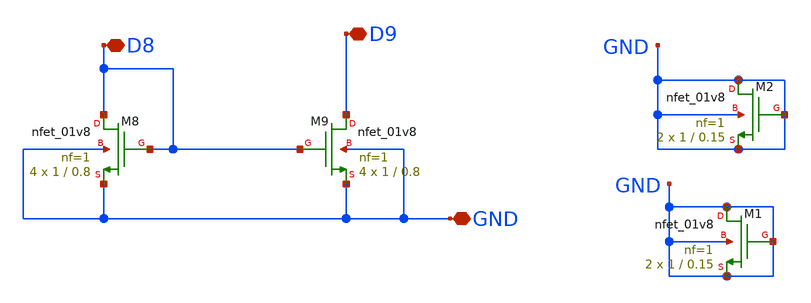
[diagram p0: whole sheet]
** sch_path: opamp/mag/nmos89.sch
**.subckt nmos89 GND D9 D8
*.iopin GND
*.iopin D9
*.iopin D8
XM8 D8 D8 GND GND sky130_fd_pr__nfet_01v8 L=0.8 W=1 nf=1 ad='int((nf+1)/2) * W/nf * 0.29' as='int((nf+2)/2) * W/nf * 0.29'
+ pd='2*int((nf+1)/2) * (W/nf + 0.29)' ps='2*int((nf+2)/2) * (W/nf + 0.29)' nrd='0.29 / W' nrs='0.29 / W'
+ sa=0 sb=0 sd=0 mult=4 m=4
XM9 D9 D8 GND GND sky130_fd_pr__nfet_01v8 L=0.8 W=1 nf=1 ad='int((nf+1)/2) * W/nf * 0.29' as='int((nf+2)/2) * W/nf * 0.29'
+ pd='2*int((nf+1)/2) * (W/nf + 0.29)' ps='2*int((nf+2)/2) * (W/nf + 0.29)' nrd='0.29 / W' nrs='0.29 / W'
+ sa=0 sb=0 sd=0 mult=4 m=4
XM1 GND GND GND GND sky130_fd_pr__nfet_01v8 L=0.15 W=1 nf=1 ad='int((nf+1)/2) * W/nf * 0.29' as='int((nf+2)/2) * W/nf * 0.29'
+ pd='2*int((nf+1)/2) * (W/nf + 0.29)' ps='2*int((nf+2)/2) * (W/nf + 0.29)' nrd='0.29 / W' nrs='0.29 / W'
+ sa=0 sb=0 sd=0 mult=2 m=2
XM2 GND GND GND GND sky130_fd_pr__nfet_01v8 L=0.15 W=1 nf=1 ad='int((nf+1)/2) * W/nf * 0.29' as='int((nf+2)/2) * W/nf * 0.29'
+ pd='2*int((nf+1)/2) * (W/nf + 0.29)' ps='2*int((nf+2)/2) * (W/nf + 0.29)' nrd='0.29 / W' nrs='0.29 / W'
+ sa=0 sb=0 sd=0 mult=2 m=2
**.ends
.end
